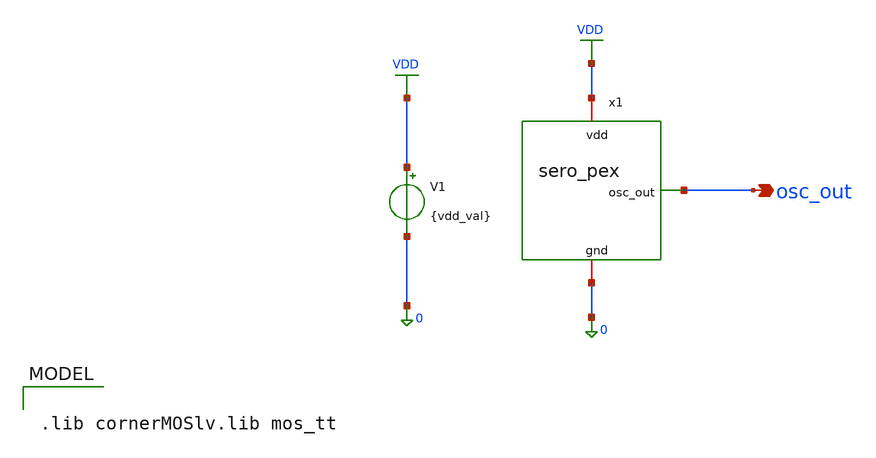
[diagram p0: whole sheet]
** sch_path: simulations/tb/vdd_v_freq_pex.sch
**.subckt vdd_v_freq_pex osc_out
*.opin osc_out
x1 VDD osc_out 0 sero_pex
V1 VDD 0 {vdd_val}
**** begin user architecture code

.lib cornerMOSlv.lib mos_tt



.param length=150n
.param vdd_val=1.2
.param temp=27
.ic v(x1.inverter_0.vin)=1.2
.include /foss/designs/sero/simulations/pex/sero.pex.spice
.control
  save all
  let v_start = 0.96
  let v_stop  = 1.44
  let v_step  = 0.06
  let n_pts   = 9
  let vdds  = vector(n_pts)
  let freqs = vector(n_pts)
  let powers = vector(n_pts)
  let idx = 0

  while idx < n_pts
    let v_curr = v_start + idx * v_step
    alterparam vdd_val = $&v_curr
    reset
    tran 2p 6n
    meas tran t1 when v(osc_out)=0.5*v_curr rise=4
    meas tran t2 when v(osc_out)=0.5*v_curr rise=5
    meas tran iavg avg i(v1) from=2n to=6n
    let freqs[idx] = 1 / (t2 - t1)
    let powers[idx] = -iavg * v_curr
    let vdds[idx]  = v_curr
    let idx = idx + 1
  end

  set curplot = control
  write vdd_v_freq_pex.raw freqs vdds powers
.endc



**** end user architecture code
**.ends

* expanding   symbol:  /foss/designs/sero/design/symbol/sero_pex.sym # of pins=3
** sym_path: design/symbol/sero.sym
.include /foss/designs/sero/simulations/pex/sero_lyt.pex.spice
.GLOBAL VDD
.end
